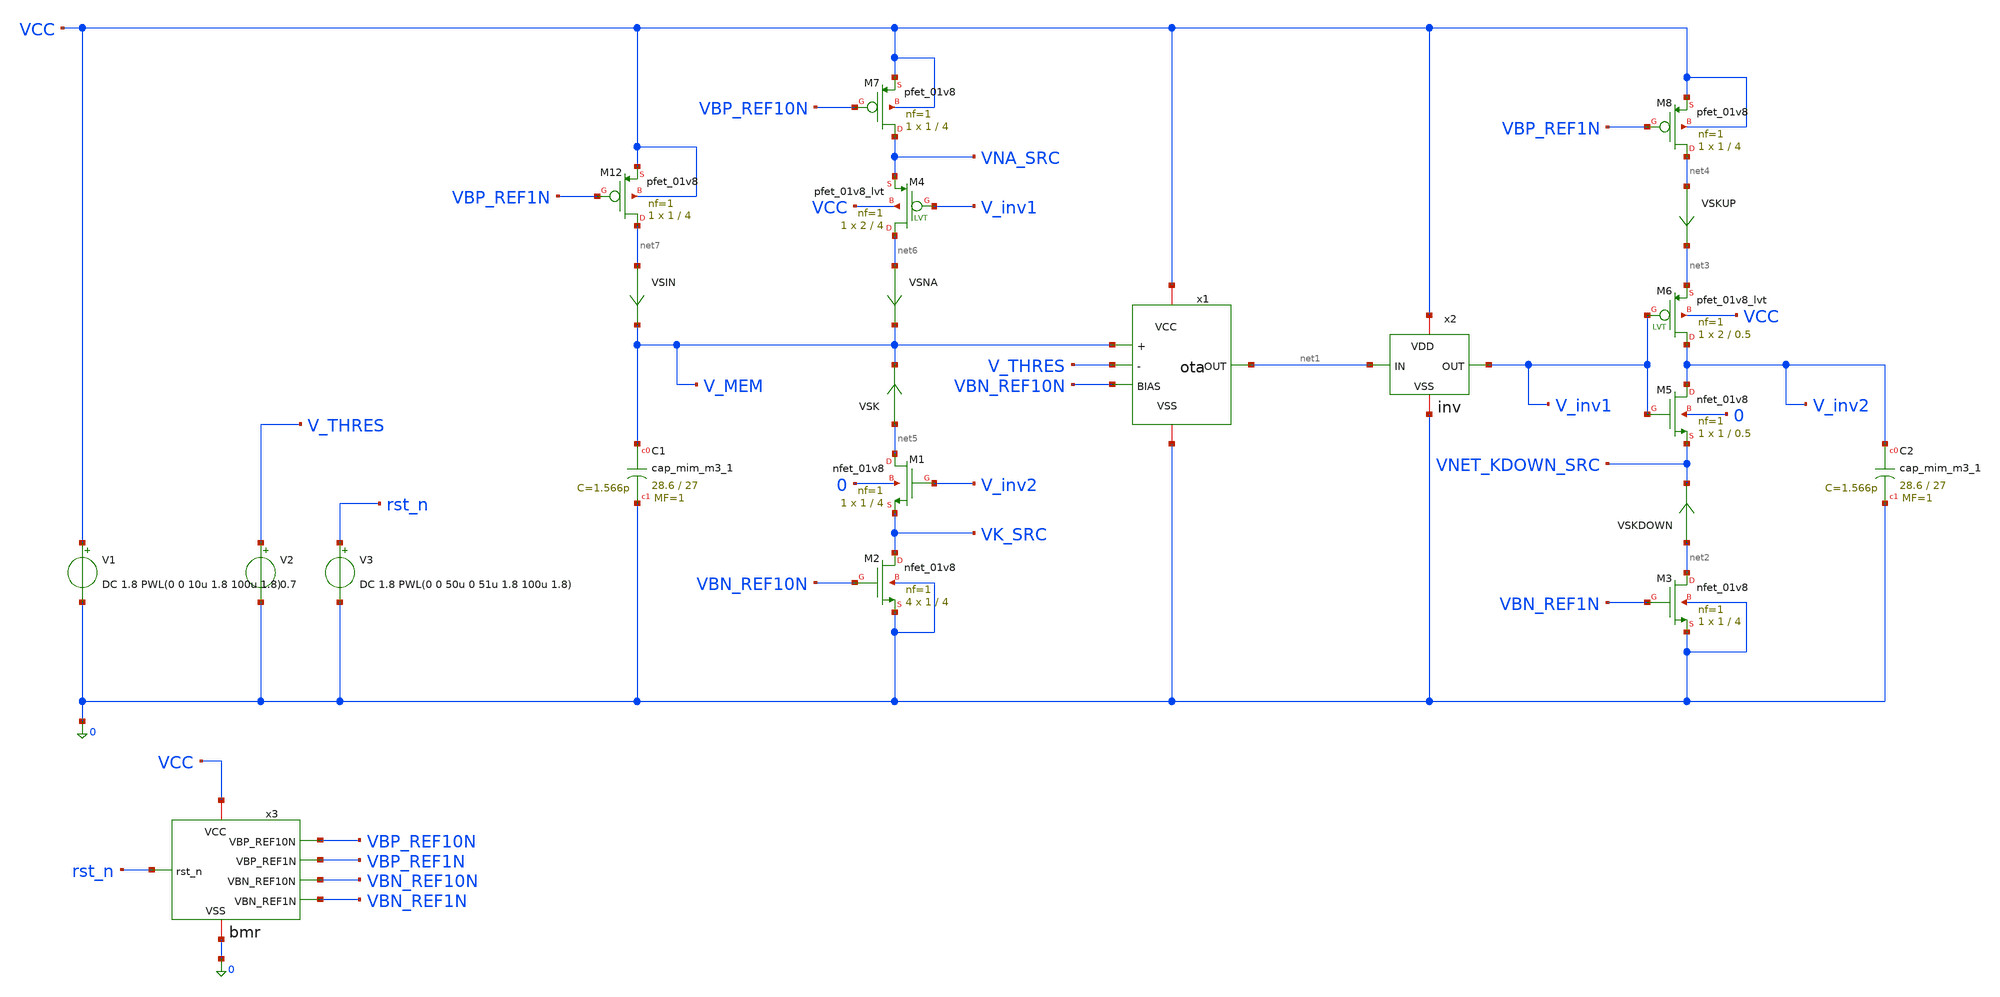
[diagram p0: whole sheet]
** sch_path: schem/vamp_if_neuron.sch
**.subckt vamp_if_neuron
x1 VCC net1 0 VBN_REF10N V_MEM V_THRES ota
x2 VCC net1 V_inv1 0 inv
XC1 V_MEM 0 sky130_fd_pr__cap_mim_m3_1 W=28.6 L=27 MF=1 m=1
XM1 net5 V_inv2 VK_SRC 0 sky130_fd_pr__nfet_01v8 L=4 W=1 nf=1 ad='int((1 + 1)/2) * 1 / 1 * 0.29' as='int((1 + 2)/2) * 1 / 1 * 0.29'
+ pd='2*int((1 + 1)/2) * (1 / 1 + 0.29)' ps='2*int((1 + 2)/2) * (1 / 1 + 0.29)' nrd='0.29 / 1 ' nrs='0.29 / 1 '
+ sa=0 sb=0 sd=0 mult=1 m=1
V1 VCC 0 DC 1.8 PWL(0 0 10u 1.8 100u 1.8)
V2 V_THRES 0 0.7
XM5 V_inv2 V_inv1 VNET_KDOWN_SRC 0 sky130_fd_pr__nfet_01v8 L=0.5 W=1 nf=1 ad='int((1 + 1)/2) * 1 / 1 * 0.29'
+ as='int((1 + 2)/2) * 1 / 1 * 0.29' pd='2*int((1 + 1)/2) * (1 / 1 + 0.29)' ps='2*int((1 + 2)/2) * (1 / 1 + 0.29)'
+ nrd='0.29 / 1 ' nrs='0.29 / 1 ' sa=0 sb=0 sd=0 mult=1 m=1
XM6 V_inv2 V_inv1 net3 VCC sky130_fd_pr__pfet_01v8_lvt L=0.5 W=2 nf=1 ad='int((1 + 1)/2) * 2 / 1 * 0.29'
+ as='int((1 + 2)/2) * 2 / 1 * 0.29' pd='2*int((1 + 1)/2) * (2 / 1 + 0.29)' ps='2*int((1 + 2)/2) * (2 / 1 + 0.29)'
+ nrd='0.29 / 2 ' nrs='0.29 / 2 ' sa=0 sb=0 sd=0 mult=1 m=1
XC2 V_inv2 0 sky130_fd_pr__cap_mim_m3_1 W=28.6 L=27 MF=1 m=1
VSNA net6 V_MEM 0
.save i(vsna)
VSKUP net4 net3 0
.save i(vskup)
VSK net5 V_MEM 0
.save i(vsk)
VSKDOWN net2 VNET_KDOWN_SRC 0
.save i(vskdown)
XM2 VK_SRC VBN_REF10N 0 0 sky130_fd_pr__nfet_01v8 L=4 W=1 nf=1 ad='int((1 + 1)/2) * 1 / 1 * 0.29' as='int((1 + 2)/2) * 1 / 1 * 0.29'
+ pd='2*int((1 + 1)/2) * (1 / 1 + 0.29)' ps='2*int((1 + 2)/2) * (1 / 1 + 0.29)' nrd='0.29 / 1 ' nrs='0.29 / 1 '
+ sa=0 sb=0 sd=0 mult=4 m=4
XM3 net2 VBN_REF1N 0 0 sky130_fd_pr__nfet_01v8 L=4 W=1 nf=1 ad='int((1 + 1)/2) * 1 / 1 * 0.29' as='int((1 + 2)/2) * 1 / 1 * 0.29'
+ pd='2*int((1 + 1)/2) * (1 / 1 + 0.29)' ps='2*int((1 + 2)/2) * (1 / 1 + 0.29)' nrd='0.29 / 1 ' nrs='0.29 / 1 '
+ sa=0 sb=0 sd=0 mult=1 m=1
XM7 VNA_SRC VBP_REF10N VCC VCC sky130_fd_pr__pfet_01v8 L=4 W=1 nf=1 ad='int((1 + 1)/2) * 1 / 1 * 0.29'
+ as='int((1 + 2)/2) * 1 / 1 * 0.29' pd='2*int((1 + 1)/2) * (1 / 1 + 0.29)' ps='2*int((1 + 2)/2) * (1 / 1 + 0.29)'
+ nrd='0.29 / 1 ' nrs='0.29 / 1 ' sa=0 sb=0 sd=0 mult=1 m=1
XM8 net4 VBP_REF1N VCC VCC sky130_fd_pr__pfet_01v8 L=4 W=1 nf=1 ad='int((1 + 1)/2) * 1 / 1 * 0.29' as='int((1 + 2)/2) * 1 / 1 * 0.29'
+ pd='2*int((1 + 1)/2) * (1 / 1 + 0.29)' ps='2*int((1 + 2)/2) * (1 / 1 + 0.29)' nrd='0.29 / 1 ' nrs='0.29 / 1 '
+ sa=0 sb=0 sd=0 mult=1 m=1
XM4 net6 V_inv1 VNA_SRC VCC sky130_fd_pr__pfet_01v8_lvt L=4 W=2 nf=1 ad='int((1 + 1)/2) * 2 / 1 * 0.29'
+ as='int((1 + 2)/2) * 2 / 1 * 0.29' pd='2*int((1 + 1)/2) * (2 / 1 + 0.29)' ps='2*int((1 + 2)/2) * (2 / 1 + 0.29)'
+ nrd='0.29 / 2 ' nrs='0.29 / 2 ' sa=0 sb=0 sd=0 mult=1 m=1
XM12 net7 VBP_REF1N VCC VCC sky130_fd_pr__pfet_01v8 L=4 W=1 nf=1 ad='int((1 + 1)/2) * 1 / 1 * 0.29' as='int((1 + 2)/2) * 1 / 1 * 0.29'
+ pd='2*int((1 + 1)/2) * (1 / 1 + 0.29)' ps='2*int((1 + 2)/2) * (1 / 1 + 0.29)' nrd='0.29 / 1 ' nrs='0.29 / 1 '
+ sa=0 sb=0 sd=0 mult=1 m=1
VSIN net7 V_MEM 0
.save i(vsin)
x3 VCC VBP_REF10N 0 VBP_REF1N VBN_REF10N VBN_REF1N rst_n bmr
V3 rst_n 0 DC 1.8 PWL(0 0 50u 0 51u 1.8 100u 1.8)
**** begin user architecture code

** opencircuitdesign pdks install
.lib $::SKYWATER_MODELS/sky130.lib.spice tt



.control

save all
tran 20n 100m uic

plot v_mem v_inv1 v_inv2
plot i(vsna) i(vsk) i(vskup) i(vskdown) ylimit -10n 10n

.endc


**** end user architecture code
**.ends

* expanding   symbol:  ota/ota.sym # of pins=6
** sym_path: schem/ota/ota.sym
** sch_path: schem/ota/ota.sch
.subckt ota VCC OUT VSS BIAS + -
*.ipin BIAS
*.ipin +
*.ipin -
*.opin OUT
*.iopin VCC
*.iopin VSS
XM1 VSRC + VBOT VSS sky130_fd_pr__nfet_01v8 L=0.5 W=1 nf=1 ad='int((1 + 1)/2) * 1 / 1 * 0.29' as='int((1 + 2)/2) * 1 / 1 * 0.29'
+ pd='2*int((1 + 1)/2) * (1 / 1 + 0.29)' ps='2*int((1 + 2)/2) * (1 / 1 + 0.29)' nrd='0.29 / 1 ' nrs='0.29 / 1 '
+ sa=0 sb=0 sd=0 mult=1 m=1
XM2 OUT - VBOT VSS sky130_fd_pr__nfet_01v8 L=0.5 W=1 nf=1 ad='int((1 + 1)/2) * 1 / 1 * 0.29' as='int((1 + 2)/2) * 1 / 1 * 0.29'
+ pd='2*int((1 + 1)/2) * (1 / 1 + 0.29)' ps='2*int((1 + 2)/2) * (1 / 1 + 0.29)' nrd='0.29 / 1 ' nrs='0.29 / 1 '
+ sa=0 sb=0 sd=0 mult=1 m=1
XM3 VSRC VSRC VCC VCC sky130_fd_pr__pfet_01v8_lvt L=0.5 W=2 nf=1 ad='int((1 + 1)/2) * 2 / 1 * 0.29' as='int((1 + 2)/2) * 2 / 1 * 0.29'
+ pd='2*int((1 + 1)/2) * (2 / 1 + 0.29)' ps='2*int((1 + 2)/2) * (2 / 1 + 0.29)' nrd='0.29 / 2 ' nrs='0.29 / 2 '
+ sa=0 sb=0 sd=0 mult=1 m=1
XM4 OUT VSRC VCC VCC sky130_fd_pr__pfet_01v8_lvt L=0.5 W=2 nf=1 ad='int((1 + 1)/2) * 2 / 1 * 0.29' as='int((1 + 2)/2) * 2 / 1 * 0.29'
+ pd='2*int((1 + 1)/2) * (2 / 1 + 0.29)' ps='2*int((1 + 2)/2) * (2 / 1 + 0.29)' nrd='0.29 / 2 ' nrs='0.29 / 2 '
+ sa=0 sb=0 sd=0 mult=1 m=1
XM5 VBOT BIAS VSS VSS sky130_fd_pr__nfet_01v8 L=0.5 W=1 nf=1 ad='int((1 + 1)/2) * 1 / 1 * 0.29' as='int((1 + 2)/2) * 1 / 1 * 0.29'
+ pd='2*int((1 + 1)/2) * (1 / 1 + 0.29)' ps='2*int((1 + 2)/2) * (1 / 1 + 0.29)' nrd='0.29 / 1 ' nrs='0.29 / 1 '
+ sa=0 sb=0 sd=0 mult=1 m=1
.ends


* expanding   symbol:  inv/inv.sym # of pins=4
** sym_path: schem/inv/inv.sym
** sch_path: schem/inv/inv.sch
.subckt inv VDD IN OUT VSS
*.ipin IN
*.iopin VDD
*.iopin VSS
*.opin OUT
XM1 OUT IN VSS VSS sky130_fd_pr__nfet_01v8 L=0.5 W=1 nf=1 ad='int((1 + 1)/2) * 1 / 1 * 0.29' as='int((1 + 2)/2) * 1 / 1 * 0.29'
+ pd='2*int((1 + 1)/2) * (1 / 1 + 0.29)' ps='2*int((1 + 2)/2) * (1 / 1 + 0.29)' nrd='0.29 / 1 ' nrs='0.29 / 1 '
+ sa=0 sb=0 sd=0 mult=1 m=1
XM2 OUT IN VDD VDD sky130_fd_pr__pfet_01v8_lvt L=0.5 W=2 nf=1 ad='int((1 + 1)/2) * 2 / 1 * 0.29' as='int((1 + 2)/2) * 2 / 1 * 0.29'
+ pd='2*int((1 + 1)/2) * (2 / 1 + 0.29)' ps='2*int((1 + 2)/2) * (2 / 1 + 0.29)' nrd='0.29 / 2 ' nrs='0.29 / 2 '
+ sa=0 sb=0 sd=0 mult=1 m=1
.ends


* expanding   symbol:  bias/bmr.sym # of pins=7
** sym_path: schem/bias/bmr.sym
** sch_path: schem/bias/bmr.sch
.subckt bmr VCC VBP_REF10N VSS VBP_REF1N VBN_REF10N VBN_REF1N rst_n
*.iopin VCC
*.iopin VSS
*.ipin rst_n
*.opin VBP_REF10N
*.opin VBP_REF1N
*.opin VBN_REF10N
*.opin VBN_REF1N
x1 VCC VBP_REF10N VSS VBN_REF10N rst_n bmr_10n
XM1 net1 VBP_REF10N VCC VCC sky130_fd_pr__pfet_01v8 L=4 W=1 nf=1 ad='int((1 + 1)/2) * 1 / 1 * 0.29' as='int((1 + 2)/2) * 1 / 1 * 0.29'
+ pd='2*int((1 + 1)/2) * (1 / 1 + 0.29)' ps='2*int((1 + 2)/2) * (1 / 1 + 0.29)' nrd='0.29 / 1 ' nrs='0.29 / 1 '
+ sa=0 sb=0 sd=0 mult=1 m=1
XM2 VBN_REF1N VBN_REF1N VSS VSS sky130_fd_pr__nfet_01v8 L=4 W=1 nf=1 ad='int((1 + 1)/2) * 1 / 1 * 0.29'
+ as='int((1 + 2)/2) * 1 / 1 * 0.29' pd='2*int((1 + 1)/2) * (1 / 1 + 0.29)' ps='2*int((1 + 2)/2) * (1 / 1 + 0.29)'
+ nrd='0.29 / 1 ' nrs='0.29 / 1 ' sa=0 sb=0 sd=0 mult=10 m=10
XM3 net2 VBN_REF1N VSS VSS sky130_fd_pr__nfet_01v8 L=4 W=1 nf=1 ad='int((1 + 1)/2) * 1 / 1 * 0.29' as='int((1 + 2)/2) * 1 / 1 * 0.29'
+ pd='2*int((1 + 1)/2) * (1 / 1 + 0.29)' ps='2*int((1 + 2)/2) * (1 / 1 + 0.29)' nrd='0.29 / 1 ' nrs='0.29 / 1 '
+ sa=0 sb=0 sd=0 mult=1 m=1
XM4 VBP_REF1N VBP_REF1N VCC VCC sky130_fd_pr__pfet_01v8 L=4 W=1 nf=1 ad='int((1 + 1)/2) * 1 / 1 * 0.29'
+ as='int((1 + 2)/2) * 1 / 1 * 0.29' pd='2*int((1 + 1)/2) * (1 / 1 + 0.29)' ps='2*int((1 + 2)/2) * (1 / 1 + 0.29)'
+ nrd='0.29 / 1 ' nrs='0.29 / 1 ' sa=0 sb=0 sd=0 mult=1 m=1
Vmeas net1 VBN_REF1N 0
.save i(vmeas)
Vmeas1 VBP_REF1N net2 0
.save i(vmeas1)
.ends


* expanding   symbol:  bias/bmr_10n.sym # of pins=5
** sym_path: schem/bias/bmr_10n.sym
** sch_path: schem/bias/bmr_10n.sch
.subckt bmr_10n VCC VBP VSS VBN rst_n
*.iopin VCC
*.iopin VSS
*.ipin rst_n
*.opin VBP
*.opin VBN
XM1 VBP VBP VCC VCC sky130_fd_pr__pfet_01v8 L=4 W=1 nf=1 ad='int((1 + 1)/2) * 1 / 1 * 0.29' as='int((1 + 2)/2) * 1 / 1 * 0.29'
+ pd='2*int((1 + 1)/2) * (1 / 1 + 0.29)' ps='2*int((1 + 2)/2) * (1 / 1 + 0.29)' nrd='0.29 / 1 ' nrs='0.29 / 1 '
+ sa=0 sb=0 sd=0 mult=1 m=1
XM2 net3 VBP VCC VCC sky130_fd_pr__pfet_01v8 L=4 W=1 nf=1 ad='int((1 + 1)/2) * 1 / 1 * 0.29' as='int((1 + 2)/2) * 1 / 1 * 0.29'
+ pd='2*int((1 + 1)/2) * (1 / 1 + 0.29)' ps='2*int((1 + 2)/2) * (1 / 1 + 0.29)' nrd='0.29 / 1 ' nrs='0.29 / 1 '
+ sa=0 sb=0 sd=0 mult=1 m=1
XM3 net2 VBN net1 VSS sky130_fd_pr__nfet_01v8 L=4 W=8 nf=1 ad='int((1 + 1)/2) * 8 / 1 * 0.29' as='int((1 + 2)/2) * 8 / 1 * 0.29'
+ pd='2*int((1 + 1)/2) * (8 / 1 + 0.29)' ps='2*int((1 + 2)/2) * (8 / 1 + 0.29)' nrd='0.29 / 8 ' nrs='0.29 / 8 '
+ sa=0 sb=0 sd=0 mult=1 m=1
XM4 VBN VBN VSS VSS sky130_fd_pr__nfet_01v8 L=4 W=1 nf=1 ad='int((1 + 1)/2) * 1 / 1 * 0.29' as='int((1 + 2)/2) * 1 / 1 * 0.29'
+ pd='2*int((1 + 1)/2) * (1 / 1 + 0.29)' ps='2*int((1 + 2)/2) * (1 / 1 + 0.29)' nrd='0.29 / 1 ' nrs='0.29 / 1 '
+ sa=0 sb=0 sd=0 mult=1 m=1
XR1 net5 net1 net4 sky130_fd_pr__res_xhigh_po_0p35 L={LR} mult=1 m=1
VSRIGHT VBP net2 0
.save i(vsright)
VSLEFT net3 VBN 0
.save i(vsleft)
XM5 VBN rst_n VCC VCC sky130_fd_pr__pfet_01v8 L=4 W=1 nf=1 ad='int((1 + 1)/2) * 1 / 1 * 0.29' as='int((1 + 2)/2) * 1 / 1 * 0.29'
+ pd='2*int((1 + 1)/2) * (1 / 1 + 0.29)' ps='2*int((1 + 2)/2) * (1 / 1 + 0.29)' nrd='0.29 / 1 ' nrs='0.29 / 1 '
+ sa=0 sb=0 sd=0 mult=1 m=1
XR2 net6 net5 net4 sky130_fd_pr__res_xhigh_po_0p35 L={LR} mult=1 m=1
XR3 net7 net6 net4 sky130_fd_pr__res_xhigh_po_0p35 L={LR} mult=1 m=1
XR4 net8 net7 net4 sky130_fd_pr__res_xhigh_po_0p35 L={LR} mult=1 m=1
XR5 net9 net8 net4 sky130_fd_pr__res_xhigh_po_0p35 L={LR} mult=1 m=1
XR6 net10 net9 net4 sky130_fd_pr__res_xhigh_po_0p35 L={LR} mult=1 m=1
XR7 net11 net10 net4 sky130_fd_pr__res_xhigh_po_0p35 L={LR} mult=1 m=1
XR8 VSS net11 net4 sky130_fd_pr__res_xhigh_po_0p35 L={LR} mult=1 m=1
**** begin user architecture code


.param LR=1084/8


**** end user architecture code
.ends

.end
